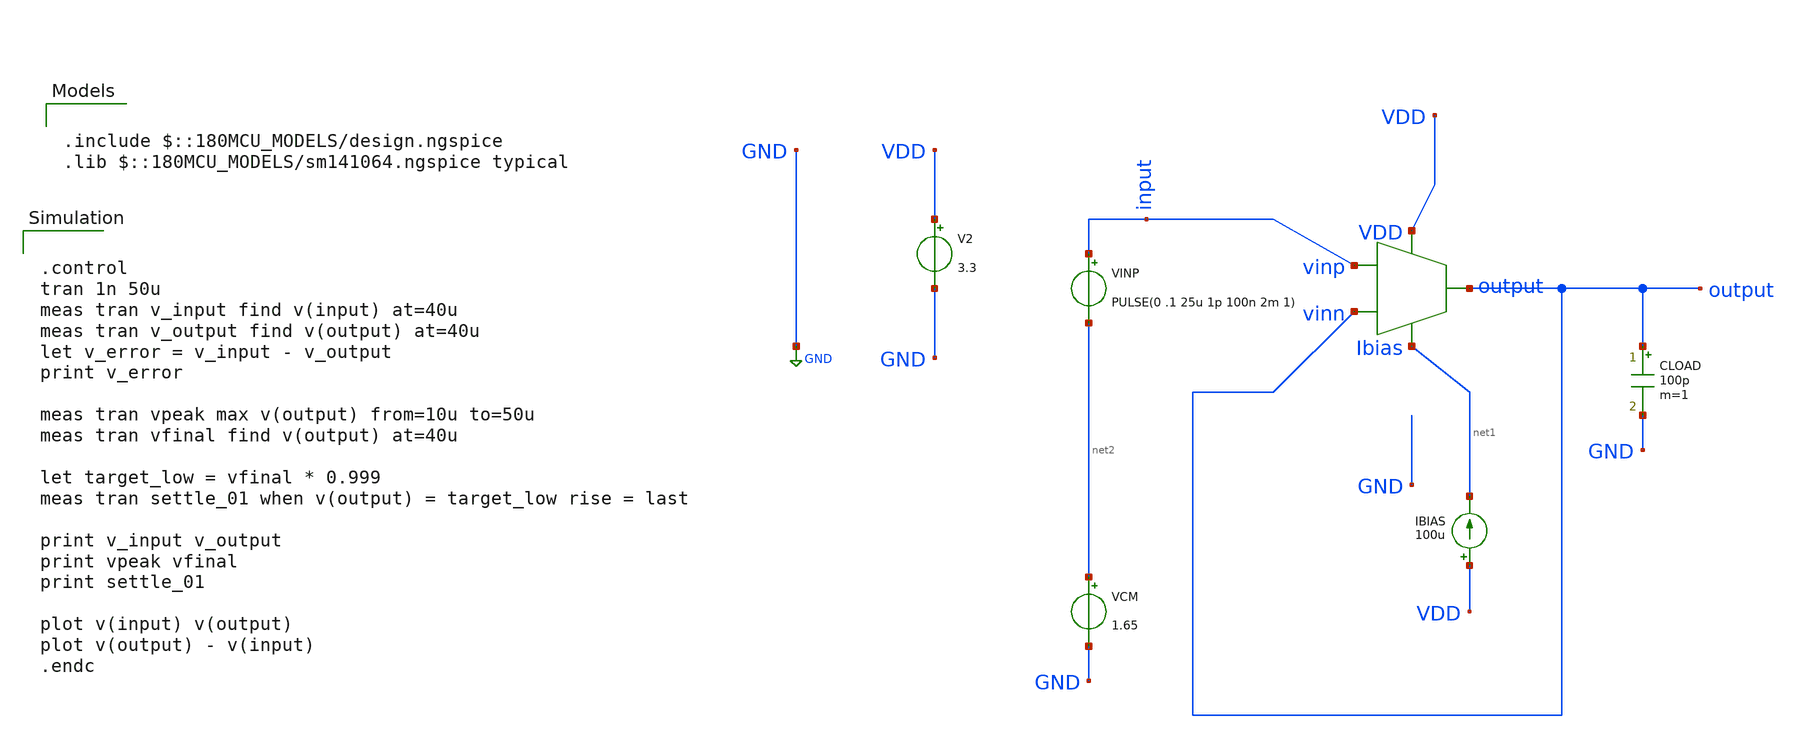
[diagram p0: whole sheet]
** sch_path: designs/libs/core_amps/ota_telescopic/telescopic_small_step_settling_tb.sch
**.subckt telescopic_small_step_settling_tb
IBIAS VDD net1 100u
V2 VDD GND 3.3
CLOAD output GND 100p m=1
VINP input net2 PULSE(0 .1 25u 1p 100n 2m 1)
VCM net2 GND 1.65
X1 input output VDD net1 output telescopic_cascode
**** begin user architecture code

.include $::180MCU_MODELS/design.ngspice
.lib $::180MCU_MODELS/sm141064.ngspice typical



.control
tran 1n 50u
meas tran v_input find v(input) at=40u
meas tran v_output find v(output) at=40u
let v_error = v_input - v_output
print v_error

meas tran vpeak max v(output) from=10u to=50u
meas tran vfinal find v(output) at=40u

let target_low = vfinal * 0.999
meas tran settle_01 when v(output) = target_low rise = last

print v_input v_output
print vpeak vfinal
print settle_01

plot v(input) v(output)
plot v(output) - v(input)
.endc


**** end user architecture code
**.ends

* expanding   symbol:  libs/core_amps/ota_telescopic/telescopic_cascode.sym # of pins=5
** sym_path: designs/libs/core_amps/ota_telescopic/telescopic_cascode.sym
** sch_path: designs/libs/core_amps/ota_telescopic/telescopic_cascode.sch
.subckt telescopic_cascode vinp vinn VDD Ibias output
*.ipin vinp
*.ipin vinn
*.opin output
*.iopin Ibias
*.iopin VDD
XM8 output net4 net3 VDD pfet_03v3 L=0.56u W=65u nf=1 ad='int((nf+1)/2) * W/nf * 0.18u' as='int((nf+2)/2) * W/nf * 0.18u'
+ pd='2*int((nf+1)/2) * (W/nf + 0.18u)' ps='2*int((nf+2)/2) * (W/nf + 0.18u)' nrd='0.18u / W' nrs='0.18u / W'
+ sa=0 sb=0 sd=0 m=4
XM4 output VBN1 net7 GND nfet_03v3 L=0.5u W=40u nf=1 ad='int((nf+1)/2) * W/nf * 0.18u' as='int((nf+2)/2) * W/nf * 0.18u'
+ pd='2*int((nf+1)/2) * (W/nf + 0.18u)' ps='2*int((nf+2)/2) * (W/nf + 0.18u)' nrd='0.18u / W' nrs='0.18u / W'
+ sa=0 sb=0 sd=0 m=1
XM1 net5 vinp net6 GND nfet_03v3 L=0.5u W=30u nf=1 ad='int((nf+1)/2) * W/nf * 0.18u' as='int((nf+2)/2) * W/nf * 0.18u'
+ pd='2*int((nf+1)/2) * (W/nf + 0.18u)' ps='2*int((nf+2)/2) * (W/nf + 0.18u)' nrd='0.18u / W' nrs='0.18u / W'
+ sa=0 sb=0 sd=0 m=1
XM2 net1 VBN1 net5 GND nfet_03v3 L=0.5u W=40u nf=1 ad='int((nf+1)/2) * W/nf * 0.18u' as='int((nf+2)/2) * W/nf * 0.18u'
+ pd='2*int((nf+1)/2) * (W/nf + 0.18u)' ps='2*int((nf+2)/2) * (W/nf + 0.18u)' nrd='0.18u / W' nrs='0.18u / W'
+ sa=0 sb=0 sd=0 m=1
XM3 net7 vinn net6 GND nfet_03v3 L=0.5u W=30u nf=1 ad='int((nf+1)/2) * W/nf * 0.18u' as='int((nf+2)/2) * W/nf * 0.18u'
+ pd='2*int((nf+1)/2) * (W/nf + 0.18u)' ps='2*int((nf+2)/2) * (W/nf + 0.18u)' nrd='0.18u / W' nrs='0.18u / W'
+ sa=0 sb=0 sd=0 m=1
XM5 net3 net1 VDD VDD pfet_03v3 L=0.56u W=65u nf=1 ad='int((nf+1)/2) * W/nf * 0.18u' as='int((nf+2)/2) * W/nf * 0.18u'
+ pd='2*int((nf+1)/2) * (W/nf + 0.18u)' ps='2*int((nf+2)/2) * (W/nf + 0.18u)' nrd='0.18u / W' nrs='0.18u / W'
+ sa=0 sb=0 sd=0 m=4
XM6 net1 net4 net2 VDD pfet_03v3 L=0.56u W=65u nf=1 ad='int((nf+1)/2) * W/nf * 0.18u' as='int((nf+2)/2) * W/nf * 0.18u'
+ pd='2*int((nf+1)/2) * (W/nf + 0.18u)' ps='2*int((nf+2)/2) * (W/nf + 0.18u)' nrd='0.18u / W' nrs='0.18u / W'
+ sa=0 sb=0 sd=0 m=4
XM7 net2 net1 VDD VDD pfet_03v3 L=0.56u W=65u nf=1 ad='int((nf+1)/2) * W/nf * 0.18u' as='int((nf+2)/2) * W/nf * 0.18u'
+ pd='2*int((nf+1)/2) * (W/nf + 0.18u)' ps='2*int((nf+2)/2) * (W/nf + 0.18u)' nrd='0.18u / W' nrs='0.18u / W'
+ sa=0 sb=0 sd=0 m=4
XM9 net6 Ibias GND GND nfet_03v3 L=0.28u W=15.54u nf=1 ad='int((nf+1)/2) * W/nf * 0.18u' as='int((nf+2)/2) * W/nf * 0.18u'
+ pd='2*int((nf+1)/2) * (W/nf + 0.18u)' ps='2*int((nf+2)/2) * (W/nf + 0.18u)' nrd='0.18u / W' nrs='0.18u / W'
+ sa=0 sb=0 sd=0 m=1
XM10 Ibias Ibias GND GND nfet_03v3 L=.28u W=5.18u nf=1 ad='int((nf+1)/2) * W/nf * 0.18u' as='int((nf+2)/2) * W/nf * 0.18u'
+ pd='2*int((nf+1)/2) * (W/nf + 0.18u)' ps='2*int((nf+2)/2) * (W/nf + 0.18u)' nrd='0.18u / W' nrs='0.18u / W'
+ sa=0 sb=0 sd=0 m=1
**** begin user architecture code


.include /foss/pdks/gf180mcuD/libs.tech/ngspice/design.ngspice
.lib /foss/pdks/gf180mcuD/libs.tech/ngspice/sm141064.ngspice typical

**** end user architecture code
V1 VBN1 GND 2.2
V2 net4 GND 1.6
.ends

.GLOBAL GND
.end
